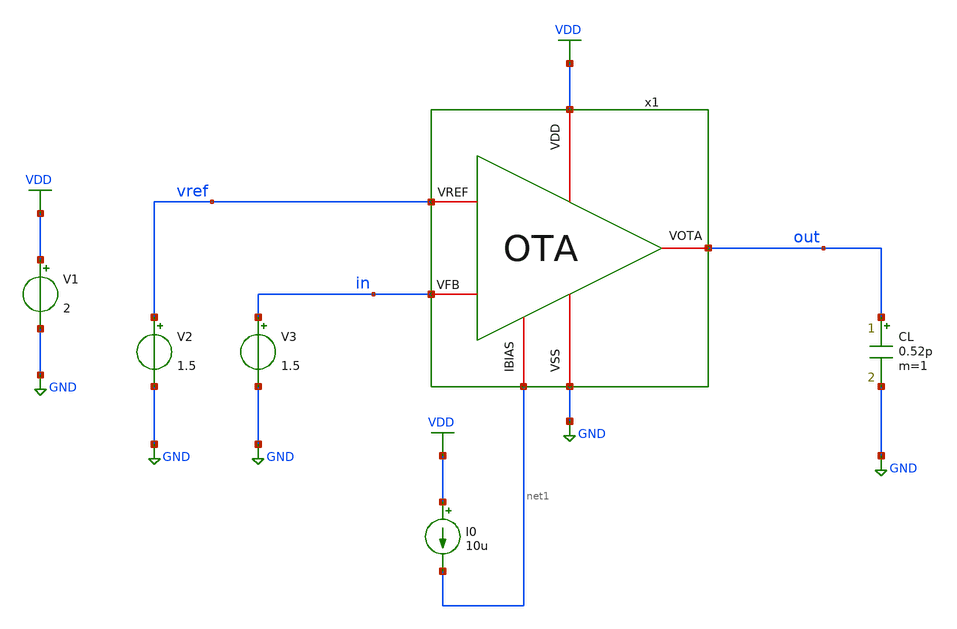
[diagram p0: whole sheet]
** sch_path: designs/libs/tb_ldo/tb_ldo/tb_ldo_OTA/tb_ldo_OTA_ac/tb_ldo_OTA_ac.sch
**.subckt tb_ldo_OTA_ac
V1 VDD GND 2
V2 vref GND 1.5
I0 VDD net1 10u
CL out GND 0.52p m=1
V3 in GND 1.5
x1 VDD vref in out net1 GND OTA
**** begin user architecture code



.control
save all

** Set sources
alter @V3[AC] = 1

** Simulations
ac dec 100 1 10G

** Plots
setplot ac1
let gain_db = db(v(out))
plot gain_db
let phase_deg = cph(v(out))*180/pi
plot phase_deg

** Measurements
meas ac DC_gain FIND gain_db AT=1Hz
let gain_3db = DC_gain-3
meas ac f_3db WHEN gain_db=$&gain_3db
meas ac f_0db WHEN gain_db=0
meas ac phase_0db FIND phase_deg WHEN gain_db=0
let phase_margin = 180 + phase_0db
print phase_margin

write tb_ldo_OTA_ac.raw

.endc
* ngspice commands




.include $::180MCU_MODELS/design.ngspice
.lib $::180MCU_MODELS/sm141064.ngspice typical
.lib $::180MCU_MODELS/sm141064.ngspice cap_mim
.lib $::180MCU_MODELS/sm141064.ngspice moscap_typical
.lib $::180MCU_MODELS/sm141064.ngspice mimcap_typical
.lib $::180MCU_MODELS/sm141064.ngspice res_typical
* .lib $::180MCU_MODELS/sm141064.ngspice res_statistical
* ngspice commands

**** end user architecture code
**.ends

* expanding   symbol:  libs/core_ldo/ldo/ldo_OTA/OTA.sym # of pins=6
** sym_path: designs/libs/core_ldo/ldo/OTA.sym
** sch_path: designs/libs/core_ldo/ldo/OTA.sch
.subckt OTA VDD VREF VFB VOTA IBIAS VSS
*.iopin VDD
*.iopin VSS
*.iopin VOTA
*.iopin VREF
*.iopin IBIAS
*.iopin VFB
XM3 net2 net2 VDD VDD pfet_05v0 L=2.00u W=8.00u nf=1 ad='int((nf+1)/2) * W/nf * 0.18u' as='int((nf+2)/2) * W/nf * 0.18u'
+ pd='2*int((nf+1)/2) * (W/nf + 0.18u)' ps='2*int((nf+2)/2) * (W/nf + 0.18u)' nrd='0.18u / W' nrs='0.18u / W'
+ sa=0 sb=0 sd=0 m=1
XM4 net3 net3 VDD VDD pfet_05v0 L=2.00u W=8.00u nf=1 ad='int((nf+1)/2) * W/nf * 0.18u' as='int((nf+2)/2) * W/nf * 0.18u'
+ pd='2*int((nf+1)/2) * (W/nf + 0.18u)' ps='2*int((nf+2)/2) * (W/nf + 0.18u)' nrd='0.18u / W' nrs='0.18u / W'
+ sa=0 sb=0 sd=0 m=1
XM5 net4 net2 VDD VDD pfet_05v0 L=2.00u W=8.00u nf=1 ad='int((nf+1)/2) * W/nf * 0.18u' as='int((nf+2)/2) * W/nf * 0.18u'
+ pd='2*int((nf+1)/2) * (W/nf + 0.18u)' ps='2*int((nf+2)/2) * (W/nf + 0.18u)' nrd='0.18u / W' nrs='0.18u / W'
+ sa=0 sb=0 sd=0 m=1
XM6 VOTA net3 VDD VDD pfet_05v0 L=2.00u W=8.00u nf=1 ad='int((nf+1)/2) * W/nf * 0.18u' as='int((nf+2)/2) * W/nf * 0.18u'
+ pd='2*int((nf+1)/2) * (W/nf + 0.18u)' ps='2*int((nf+2)/2) * (W/nf + 0.18u)' nrd='0.18u / W' nrs='0.18u / W'
+ sa=0 sb=0 sd=0 m=2
XM9 IBIAS IBIAS VSS VSS nfet_05v0 L=2.00u W=4.00u nf=1 ad='int((nf+1)/2) * W/nf * 0.18u' as='int((nf+2)/2) * W/nf * 0.18u'
+ pd='2*int((nf+1)/2) * (W/nf + 0.18u)' ps='2*int((nf+2)/2) * (W/nf + 0.18u)' nrd='0.18u / W' nrs='0.18u / W'
+ sa=0 sb=0 sd=0 m=1
XM10 net1 IBIAS VSS VSS nfet_05v0 L=2.00u W=4.00u nf=1 ad='int((nf+1)/2) * W/nf * 0.18u' as='int((nf+2)/2) * W/nf * 0.18u'
+ pd='2*int((nf+1)/2) * (W/nf + 0.18u)' ps='2*int((nf+2)/2) * (W/nf + 0.18u)' nrd='0.18u / W' nrs='0.18u / W'
+ sa=0 sb=0 sd=0 m=1
XM7 net4 net4 VSS VSS nfet_05v0 L=2.00u W=4.00u nf=1 ad='int((nf+1)/2) * W/nf * 0.18u' as='int((nf+2)/2) * W/nf * 0.18u'
+ pd='2*int((nf+1)/2) * (W/nf + 0.18u)' ps='2*int((nf+2)/2) * (W/nf + 0.18u)' nrd='0.18u / W' nrs='0.18u / W'
+ sa=0 sb=0 sd=0 m=1
XM8 VOTA net4 VSS VSS nfet_05v0 L=2.00u W=4.00u nf=1 ad='int((nf+1)/2) * W/nf * 0.18u' as='int((nf+2)/2) * W/nf * 0.18u'
+ pd='2*int((nf+1)/2) * (W/nf + 0.18u)' ps='2*int((nf+2)/2) * (W/nf + 0.18u)' nrd='0.18u / W' nrs='0.18u / W'
+ sa=0 sb=0 sd=0 m=2
XM1 net2 VREF net1 net1 nfet_05v0 L=0.60u W=40.00u nf=1 ad='int((nf+1)/2) * W/nf * 0.18u' as='int((nf+2)/2) * W/nf * 0.18u'
+ pd='2*int((nf+1)/2) * (W/nf + 0.18u)' ps='2*int((nf+2)/2) * (W/nf + 0.18u)' nrd='0.18u / W' nrs='0.18u / W'
+ sa=0 sb=0 sd=0 m=1
XM2 net3 VFB net1 net1 nfet_05v0 L=0.60u W=40.00u nf=1 ad='int((nf+1)/2) * W/nf * 0.18u' as='int((nf+2)/2) * W/nf * 0.18u'
+ pd='2*int((nf+1)/2) * (W/nf + 0.18u)' ps='2*int((nf+2)/2) * (W/nf + 0.18u)' nrd='0.18u / W' nrs='0.18u / W'
+ sa=0 sb=0 sd=0 m=1
.ends

.GLOBAL GND
.GLOBAL VDD
.end
